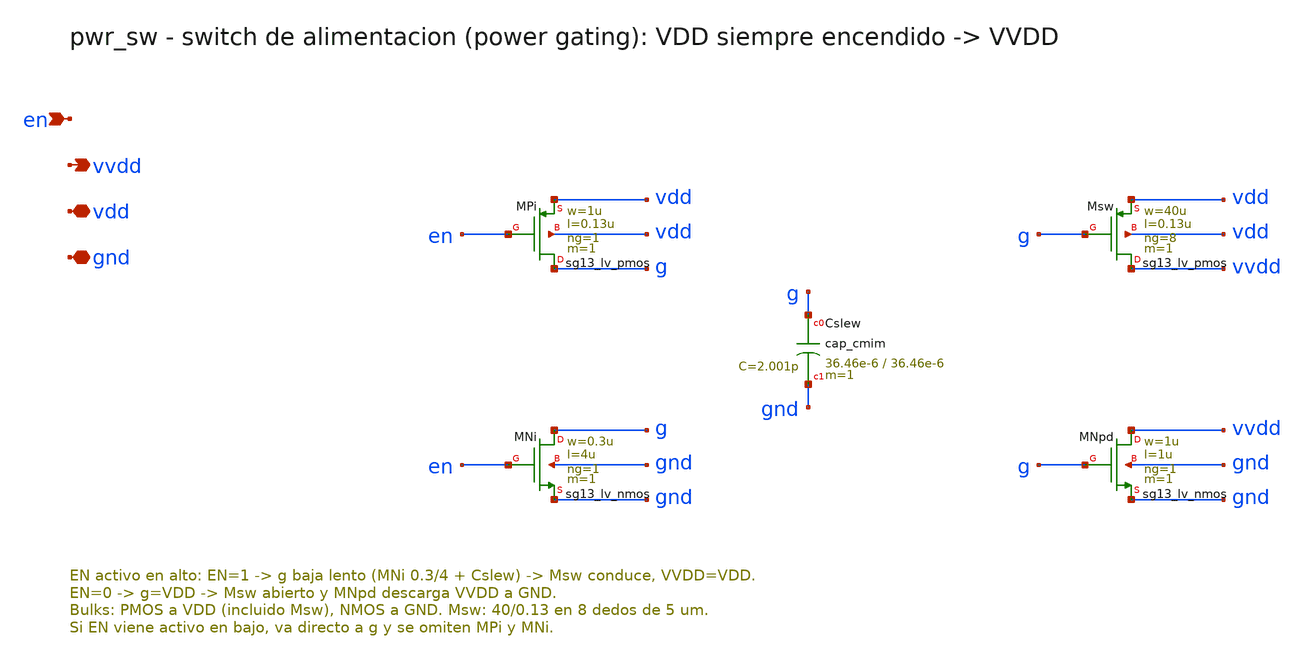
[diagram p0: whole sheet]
** sch_path: Enfoque_B/xschem/celdas/pwr_sw.sch
**.subckt pwr_sw en vvdd vdd gnd
*.ipin en
*.opin vvdd
*.iopin vdd
*.iopin gnd
XMPi g en vdd vdd sg13_lv_pmos w=1u l=0.13u ng=1 m=1 mm_ok=1
XMNi g en gnd gnd sg13_lv_nmos w=0.3u l=4u ng=1 m=1 mm_ok=1
XCslew g gnd cap_cmim w=36.46e-6 l=36.46e-6 m=1 mm_ok=1
XMsw vvdd g vdd vdd sg13_lv_pmos w=40u l=0.13u ng=8 m=1 mm_ok=1
XMNpd vvdd g gnd gnd sg13_lv_nmos w=1u l=1u ng=1 m=1 mm_ok=1
**.ends
.end
